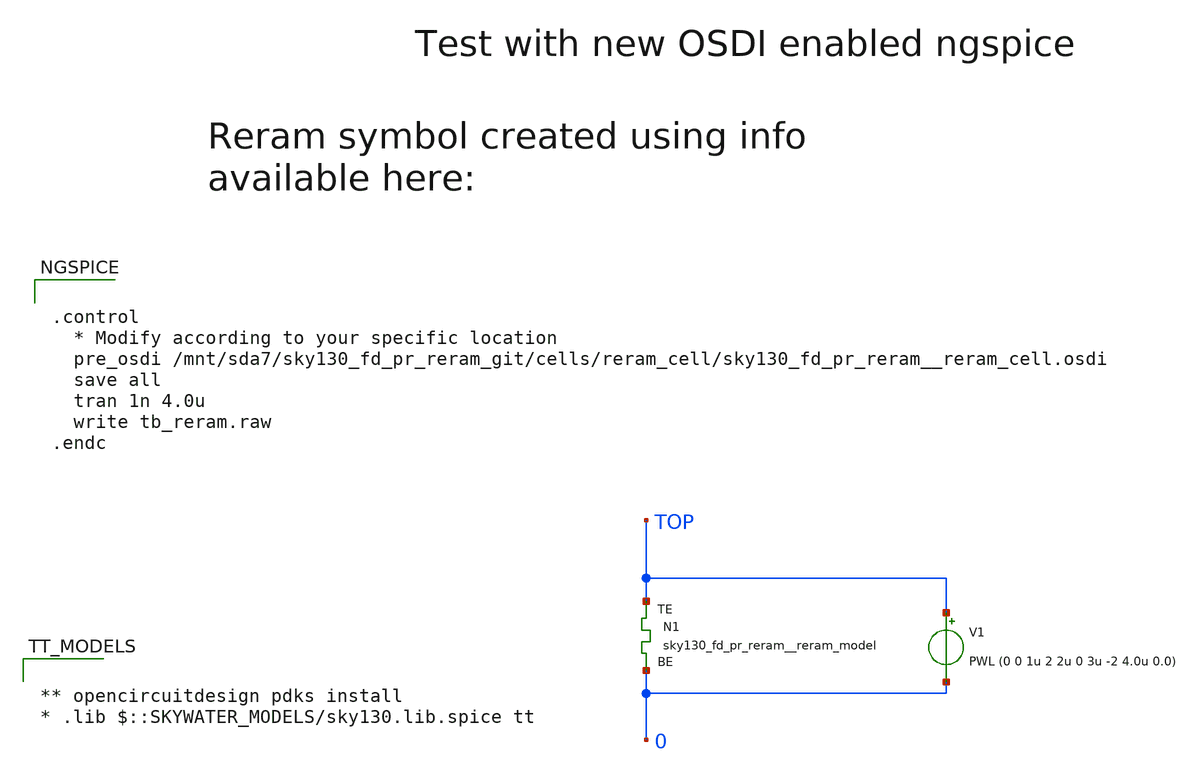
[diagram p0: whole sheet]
** sch_path: sky130_tests/tb_reram.sch
* Copyright 2021 Stefan Frederik Schippers
* Licensed under the Apache License, Version 2.0 (the "License");
* you may not use this file except in compliance with the License.
* You may obtain a copy of the License at
* https://www.apache.org/licenses/LICENSE-2.0
* Unless required by applicable law or agreed to in writing, software
* distributed under the License is distributed on an "AS IS" BASIS,
* WITHOUT WARRANTIES OR CONDITIONS OF ANY KIND, either express or implied.
* See the License for the specific language governing permissions and
* limitations under the License.
**.subckt tb_reram
N1 TOP 0 sky130_fd_pr_reram__reram_model
V1 TOP 0 PWL (0 0 1u 2 2u 0 3u -2 4.0u 0.0)
**** begin user architecture code


.control
  * Modify according to your specific location
  pre_osdi /mnt/sda7/sky130_fd_pr_reram_git/cells/reram_cell/sky130_fd_pr_reram__reram_cell.osdi
  save all
  tran 1n 4.0u
  write tb_reram.raw
.endc




** opencircuitdesign pdks install
* .lib $::SKYWATER_MODELS/sky130.lib.spice tt

**** end user architecture code
**.ends
**** begin user architecture code

.model sky130_fd_pr_reram__reram_model sky130_fd_pr_reram__reram_cell area_ox=0.1024e-12  Tox=5.0e-9
+  Tfilament_max=4.9e-9  Tfilament_min=3.3e-9  Tfilament_0=3.5e-9  Eact_generation=1.501  Eact_recombination=1.500
+  I_k1=6.140e-5  Tfilament_ref=4.7249e-9  V_ref=0.430  velocity_k1=150  gamma_k0=16.5  gamma_k1=-1.25
+   Temperature_0=300  C_thermal=3.1825e-16  tau_thermal=0.23e-9  t_step=1.0e-9

**** end user architecture code
.end
